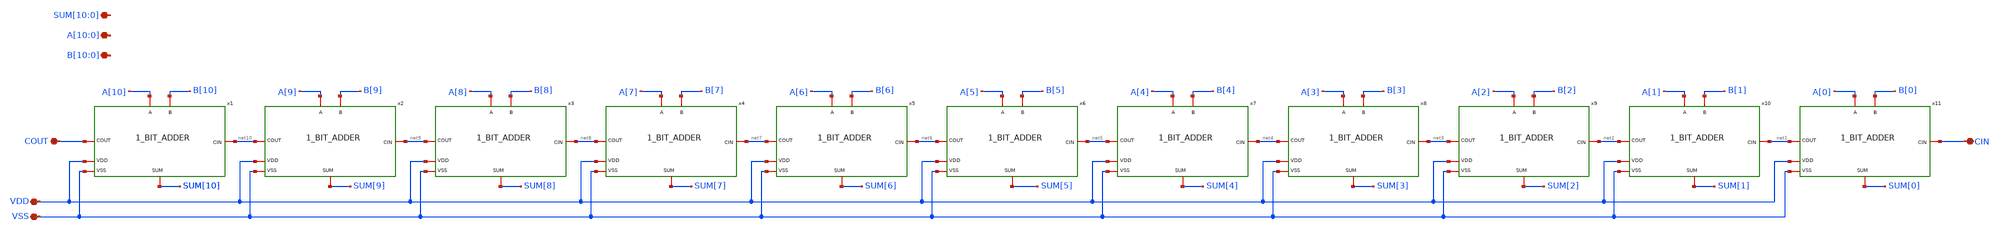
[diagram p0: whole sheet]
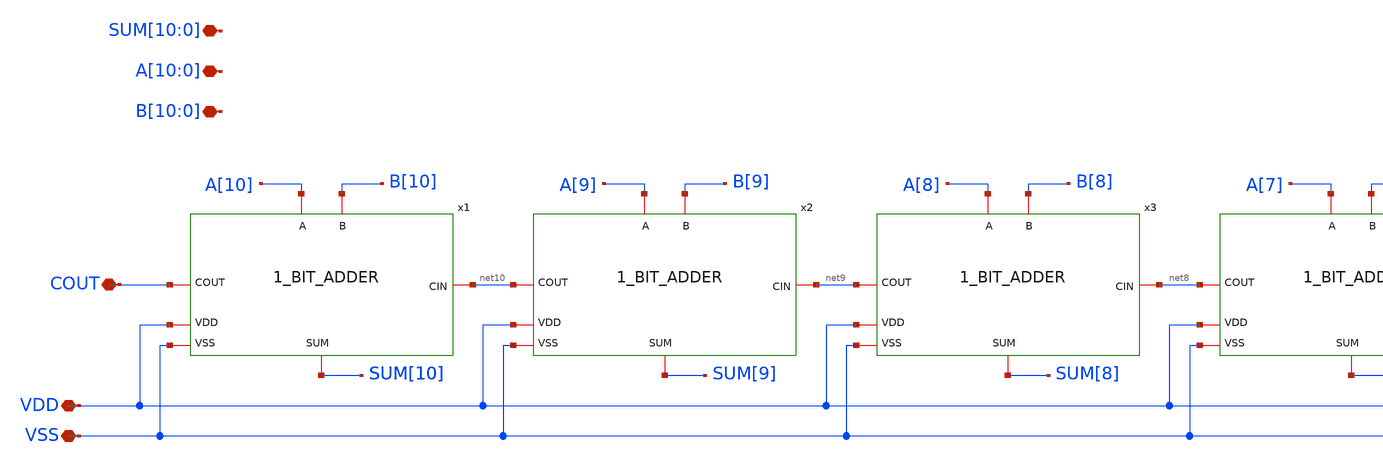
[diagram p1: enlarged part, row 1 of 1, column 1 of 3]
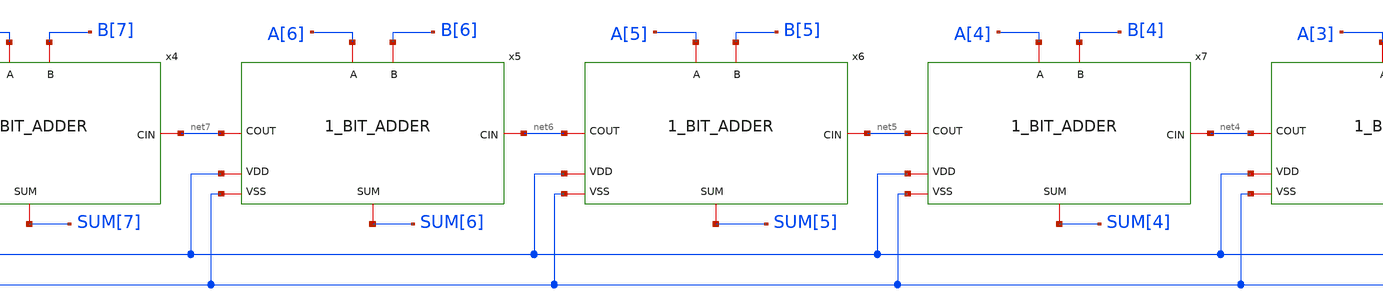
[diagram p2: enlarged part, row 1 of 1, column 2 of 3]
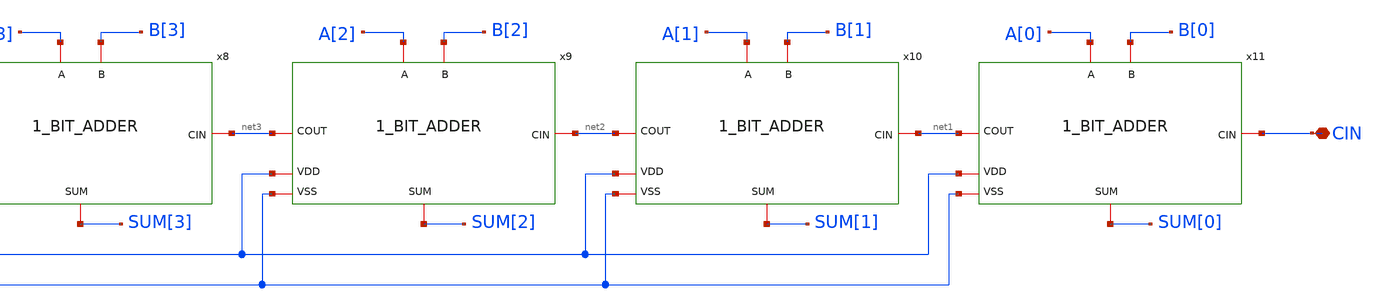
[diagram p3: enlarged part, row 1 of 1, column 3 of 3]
** sch_path: design/CNR_GR03_SKY130NM/11_BIT_ADDER.sch
**.subckt 11_BIT_ADDER VDD VSS
*+ SUM[10],SUM[9],SUM[8],SUM[7],SUM[6],SUM[5],SUM[4],SUM[3],SUM[2],SUM[1],SUM[0] A[10],A[9],A[8],A[7],A[6],A[5],A[4],A[3],A[2],A[1],A[0]
*+ B[10],B[9],B[8],B[7],B[6],B[5],B[4],B[3],B[2],B[1],B[0] COUT CIN
*.iopin VDD
*.iopin VSS
*.iopin SUM[10],SUM[9],SUM[8],SUM[7],SUM[6],SUM[5],SUM[4],SUM[3],SUM[2],SUM[1],SUM[0]
*.iopin A[10],A[9],A[8],A[7],A[6],A[5],A[4],A[3],A[2],A[1],A[0]
*.iopin B[10],B[9],B[8],B[7],B[6],B[5],B[4],B[3],B[2],B[1],B[0]
*.iopin COUT
*.iopin CIN
x1 VDD A[10] SUM[10] B[10] net10 COUT VSS 1_BIT_ADDER
x2 VDD A[9] SUM[9] B[9] net9 net10 VSS 1_BIT_ADDER
x3 VDD A[8] SUM[8] B[8] net8 net9 VSS 1_BIT_ADDER
x4 VDD A[7] SUM[7] B[7] net7 net8 VSS 1_BIT_ADDER
x5 VDD A[6] SUM[6] B[6] net6 net7 VSS 1_BIT_ADDER
x6 VDD A[5] SUM[5] B[5] net5 net6 VSS 1_BIT_ADDER
x7 VDD A[4] SUM[4] B[4] net4 net5 VSS 1_BIT_ADDER
x8 VDD A[3] SUM[3] B[3] net3 net4 VSS 1_BIT_ADDER
x9 VDD A[2] SUM[2] B[2] net2 net3 VSS 1_BIT_ADDER
x10 VDD A[1] SUM[1] B[1] net1 net2 VSS 1_BIT_ADDER
x11 VDD A[0] SUM[0] B[0] CIN net1 VSS 1_BIT_ADDER
**.ends
.end
